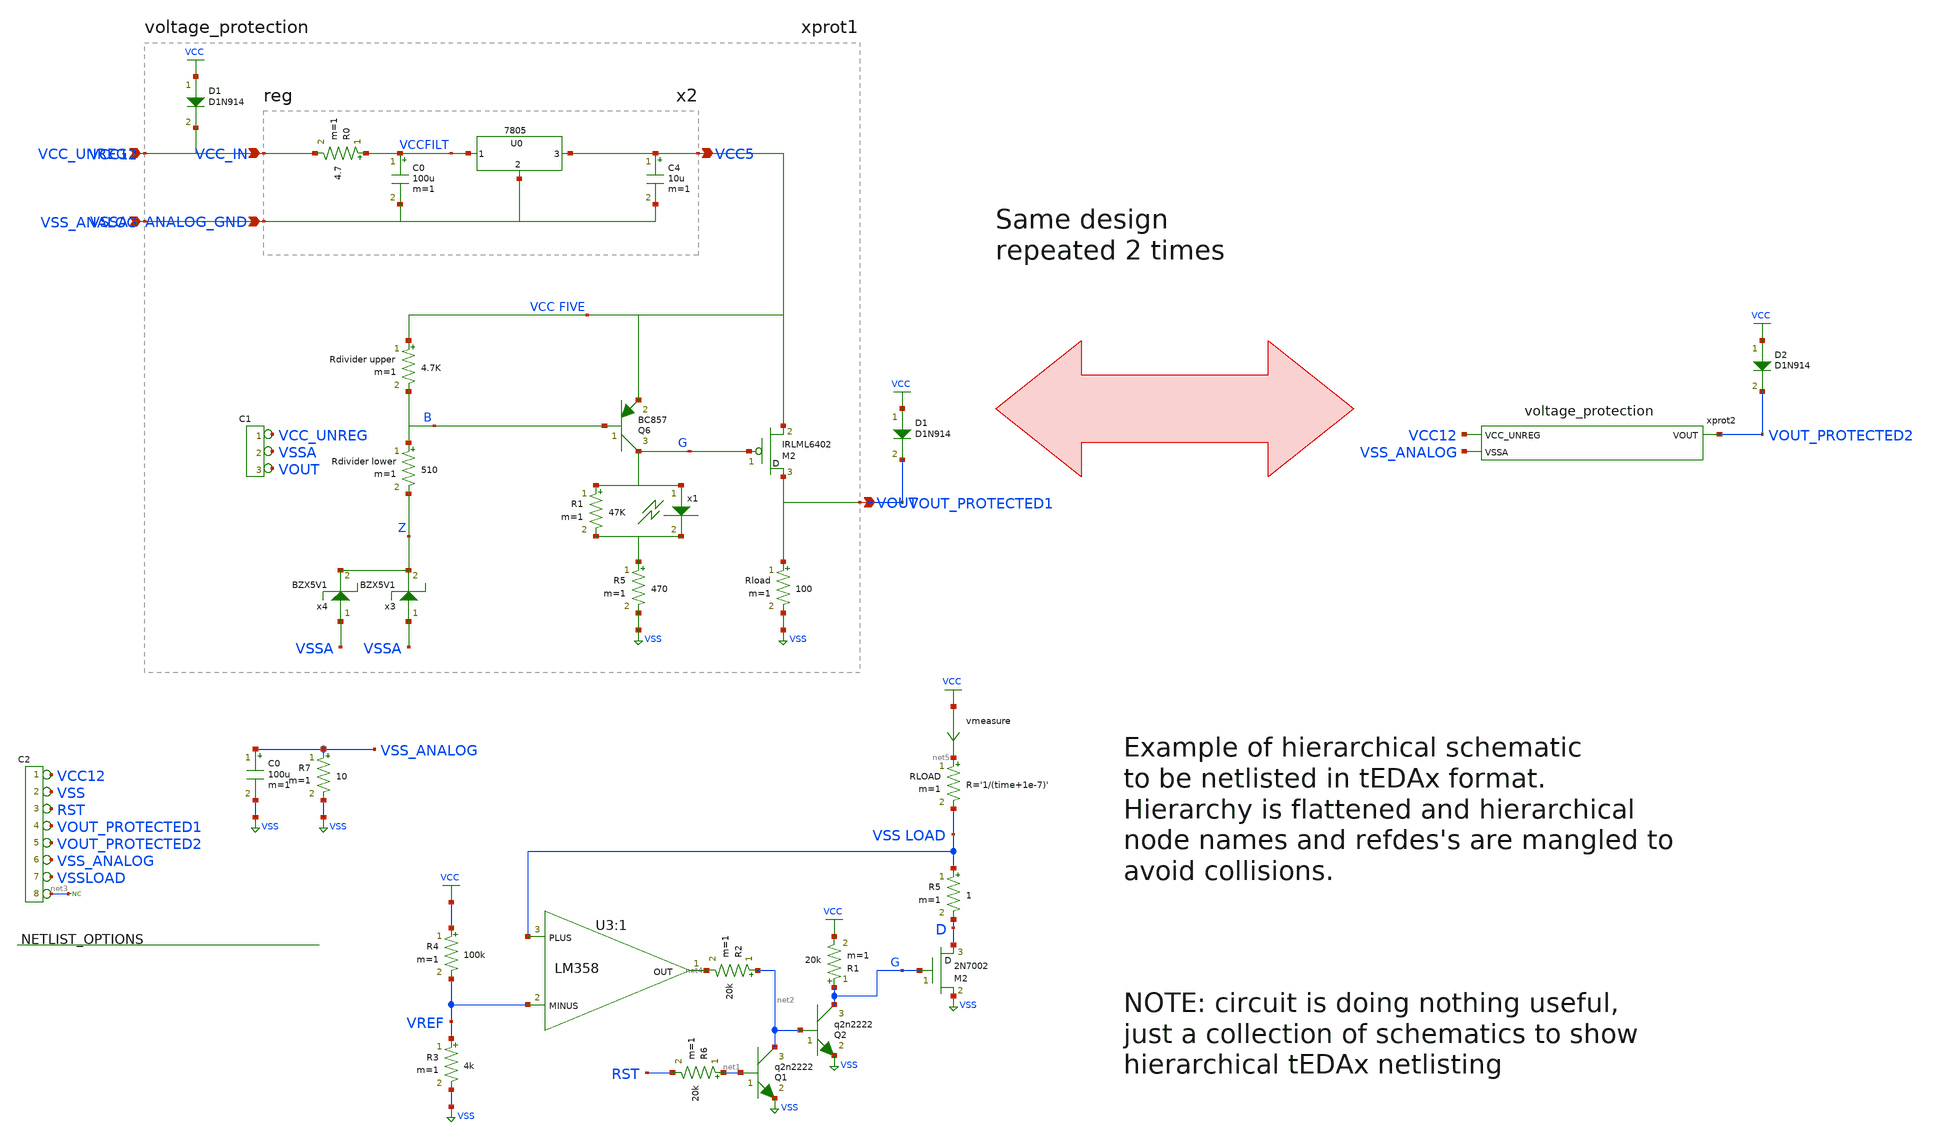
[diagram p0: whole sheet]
** sch_path: xschem_library/pcb/hierarchical_tedax.sch
**.subckt hierarchical_tedax
*connector(8,1) ?1 VCC12 ?1 VSS ?1 RST ?1 VOUT_PROTECTED1 ?1 VOUT_PROTECTED2 ?1 VSS_ANALOG ?1
*+ VSSLOAD ?1 net3
XU3:1 VSS LOAD VREF VCC VSS net4 LM358
R3 VREF VSS 4k m=1
R4 VCC VREF 100k m=1
XM2 D G VSS M2N7002 m=1
R5 VSS LOAD D 1 m=1
xprot1 VCC12 VSS_ANALOG VOUT_PROTECTED1 voltage_protection
RLOAD net5 VSS LOAD R='1/(time+1e-7)' m=1
vmeasure VCC net5 0
.save i(vmeasure)
R2 net2 net4 20k m=1
Q1 net2 net1 VSS q2n2222 area=1 m=1
R6 net1 RST 20k m=1
Q2 G net2 VSS q2n2222 area=1 m=1
R1 G VCC 20k m=1
D1 VCC VOUT_PROTECTED1 D1N914 area=1
R7 VSS_ANALOG VSS 10 m=1
C0 VSS_ANALOG VSS 100u m=1
* noconn #net3
xprot2 VCC12 VSS_ANALOG VOUT_PROTECTED2 voltage_protection
D2 VCC VOUT_PROTECTED2 D1N914 area=1
**.ends

* expanding   symbol:  voltage_protection.sch # of pins=3
** sym_path: xschem_library/pcb/voltage_protection.sch
** sch_path: xschem_library/pcb/voltage_protection.sch
.subckt voltage_protection VCC_UNREG VSSA VOUT
*.opin VOUT
*.ipin VCC_UNREG
*.ipin VSSA
*connector(3,1) ?1 VCC_UNREG ?1 VSSA ?1 VOUT
Rload VOUT VSS 100 m=1
Q6 G B VCC FIVE BC857 area=1 m=1
x3 VSSA Z BZX5V1
Rdivider upper VCC FIVE B 4.7K m=1
R5 net1 VSS 470 m=1
Rdivider lower B Z 510 m=1
XM2 VOUT G VCC FIVE IRLML6402 m=1
x1 G net1 D1N5765
R1 G net1 47K m=1
x2 VCC FIVE VCC_UNREG VSSA reg
D1 VCC VCC_UNREG D1N914 area=1
.ends


* expanding   symbol:  reg.sch # of pins=3
** sym_path: xschem_library/pcb/reg.sch
** sch_path: xschem_library/pcb/reg.sch
.subckt reg VCC5 VCC_IN ANALOG_GND
*.opin VCC5
*.ipin VCC_IN
*.ipin ANALOG_GND
C0 VCCFILT ANALOG_GND 100u m=1
XU0 VCCFILT ANALOG_GND VCC5 7805
C4 VCC5 ANALOG_GND 10u m=1
R0 VCCFILT VCC_IN 4.7 m=1
.ends

.GLOBAL VSS
.GLOBAL VCC
.end
